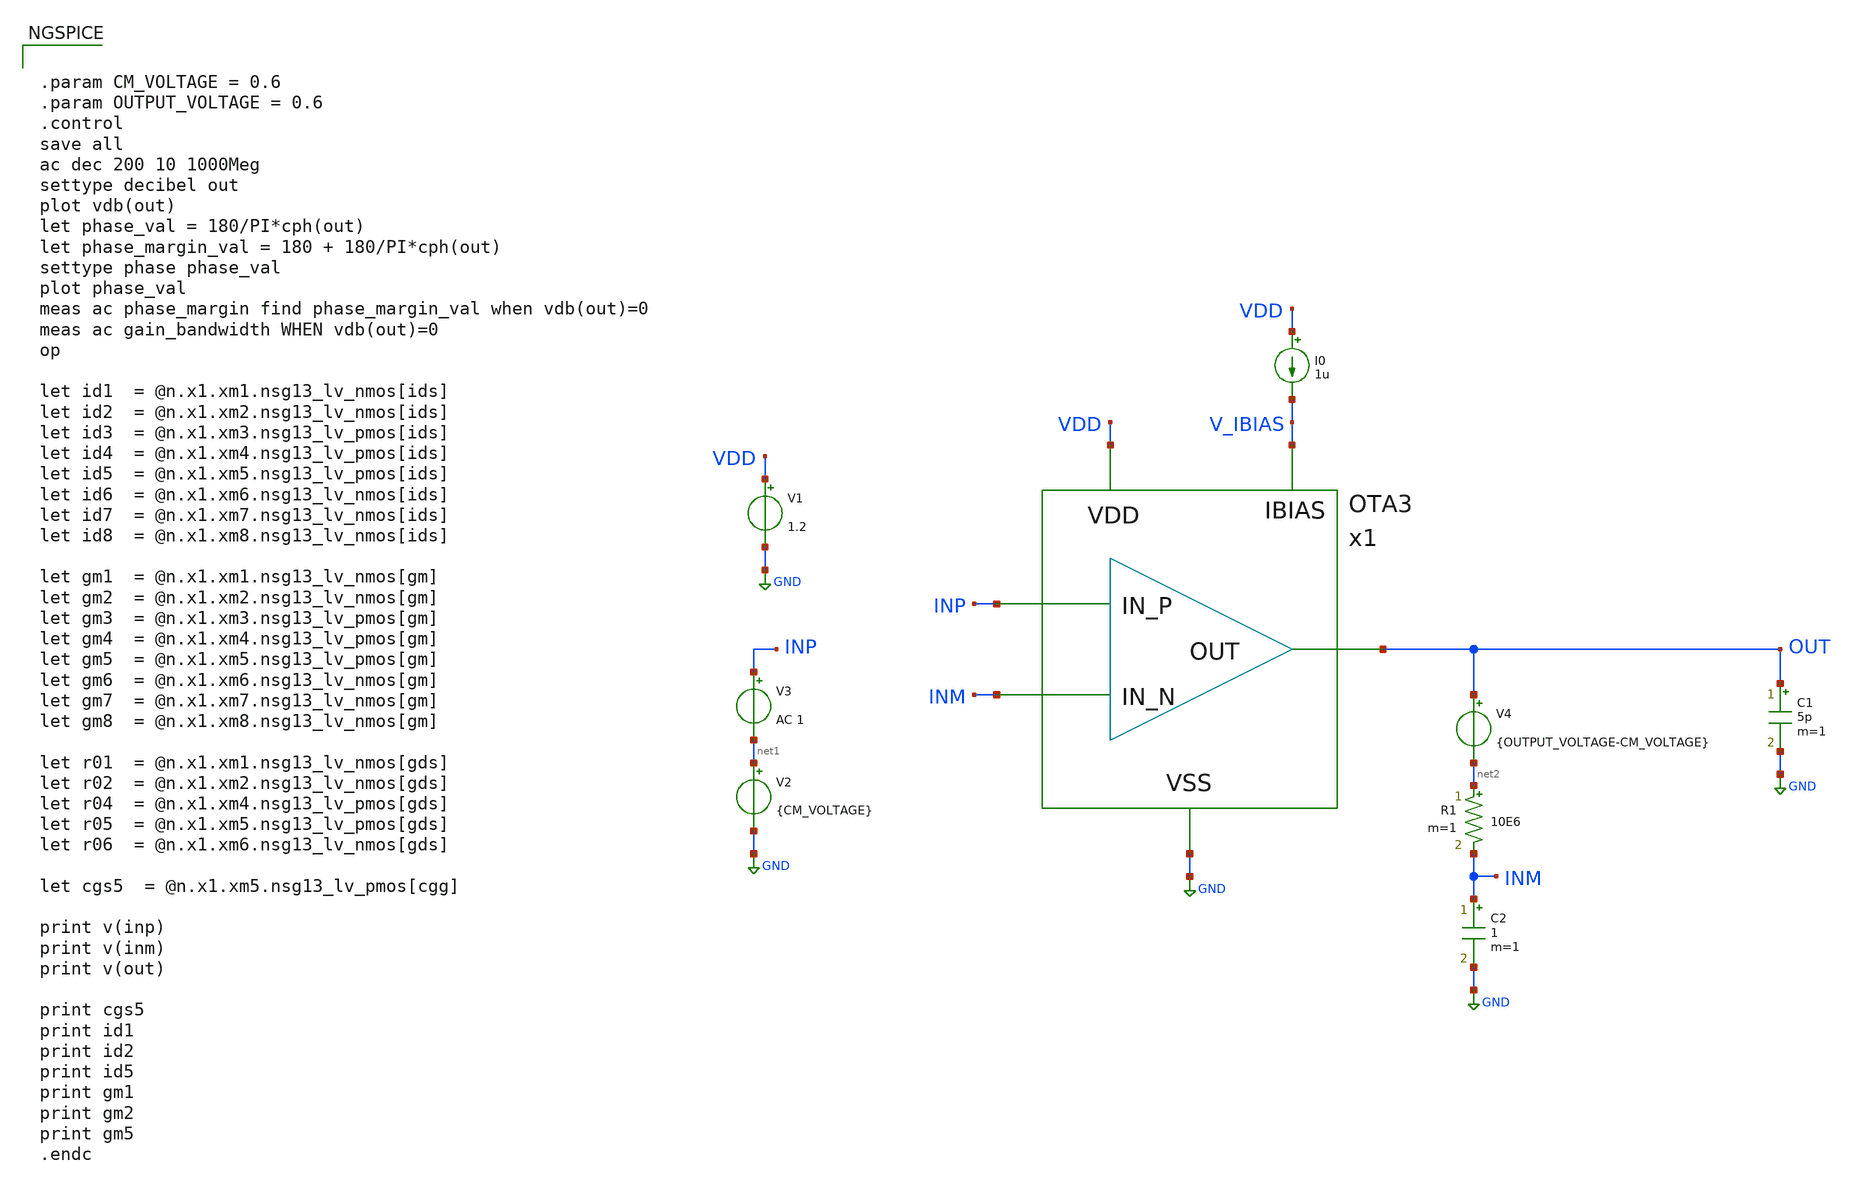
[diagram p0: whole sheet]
** sch_path: xschem/Tareas/Tarea_2/tb_OTA_lvt.sch
**.subckt tb_OTA_lvt
V1 VDD GND 1.2
I0 VDD V_IBIAS 1u
V2 net1 GND {CM_VOLTAGE}
V3 INP net1 AC 1
C1 OUT GND 5p m=1
R1 net2 INM 10E6 m=1
V4 OUT net2 {OUTPUT_VOLTAGE-CM_VOLTAGE}
C2 INM GND 1 m=1
x1 INP INM OUT VDD GND V_IBIAS OTA3
**** begin user architecture code


.param CM_VOLTAGE = 0.6
.param OUTPUT_VOLTAGE = 0.6
.control
save all
ac dec 200 10 1000Meg
settype decibel out
plot vdb(out)
let phase_val = 180/PI*cph(out)
let phase_margin_val = 180 + 180/PI*cph(out)
settype phase phase_val
plot phase_val
meas ac phase_margin find phase_margin_val when vdb(out)=0
meas ac gain_bandwidth WHEN vdb(out)=0
op

let id1  = @n.x1.xm1.nsg13_lv_nmos[ids]
let id2  = @n.x1.xm2.nsg13_lv_nmos[ids]
let id3  = @n.x1.xm3.nsg13_lv_pmos[ids]
let id4  = @n.x1.xm4.nsg13_lv_pmos[ids]
let id5  = @n.x1.xm5.nsg13_lv_pmos[ids]
let id6  = @n.x1.xm6.nsg13_lv_nmos[ids]
let id7  = @n.x1.xm7.nsg13_lv_nmos[ids]
let id8  = @n.x1.xm8.nsg13_lv_nmos[ids]

let gm1  = @n.x1.xm1.nsg13_lv_nmos[gm]
let gm2  = @n.x1.xm2.nsg13_lv_nmos[gm]
let gm3  = @n.x1.xm3.nsg13_lv_pmos[gm]
let gm4  = @n.x1.xm4.nsg13_lv_pmos[gm]
let gm5  = @n.x1.xm5.nsg13_lv_pmos[gm]
let gm6  = @n.x1.xm6.nsg13_lv_nmos[gm]
let gm7  = @n.x1.xm7.nsg13_lv_nmos[gm]
let gm8  = @n.x1.xm8.nsg13_lv_nmos[gm]

let r01  = @n.x1.xm1.nsg13_lv_nmos[gds]
let r02  = @n.x1.xm2.nsg13_lv_nmos[gds]
let r04  = @n.x1.xm4.nsg13_lv_pmos[gds]
let r05  = @n.x1.xm5.nsg13_lv_pmos[gds]
let r06  = @n.x1.xm6.nsg13_lv_nmos[gds]

let cgs5  = @n.x1.xm5.nsg13_lv_pmos[cgg]

print v(inp)
print v(inm)
print v(out)

print cgs5
print id1
print id2
print id5
print gm1
print gm2
print gm5
.endc




.lib cornerMOShv.lib mos_tt
.lib cornerMOSlv.lib mos_tt
*.lib cornerMOShv.lib mos_ff
*.lib cornerMOSlv.lib mos_ff
*.lib cornerMOShv.lib mos_ss
*.lib cornerMOSlv.lib mos_ss
*.lib cornerMOShv.lib mos_sf
*.lib cornerMOSlv.lib mos_sf
*.lib cornerMOShv.lib mos_fs
*.lib cornerMOSlv.lib mos_fs

.include /opt/pdks/ihp-sg13g2/libs.ref/sg13g2_stdcell/spice/sg13g2_stdcell.spice
.lib $::SG13G2_MODELS/cornerRES.lib res_typ
.lib $::SG13G2_MODELS/cornerCAP.lib cap_typ
*.lib $::SG13G2_MODELS/diodes.lib

**** end user architecture code
**.ends

* expanding   symbol:  OTA3.sym # of pins=6
** sym_path: xschem/Tareas/Tarea_2/OTA3.sym
** sch_path: xschem/Tareas/Tarea_2/OTA3.sch
.subckt OTA3 IN_P IN_N OUT VDD VSS ibias
*.ipin IN_N
*.ipin IN_P
*.opin OUT
*.ipin VDD
*.ipin VSS
*.ipin ibias
C2 OUT Vo1_p 1p m=1
XM8 ibias ibias VSS VSS sg13_lv_nmos w=1u l=0.5u ng=1 m=1 mm_ok=1
XM7 Vsrc ibias VSS VSS sg13_lv_nmos w=1.5u l=0.5u ng=1 m=1 mm_ok=1
XM6 OUT ibias VSS VSS sg13_lv_nmos w=1u l=0.5u ng=1 m=5 mm_ok=1
XM1 Vo1_n IN_N Vsrc VSS sg13_lv_nmos w=1u l=0.5u ng=1 m=1 mm_ok=1
XM2 Vo1_p IN_P Vsrc VSS sg13_lv_nmos w=1u l=0.5u ng=1 m=1 mm_ok=1
XM3 Vo1_n Vo1_n VDD VDD sg13_lv_pmos w=1u l=0.8u ng=1 m=1 mm_ok=1
XM4 Vo1_p Vo1_n VDD VDD sg13_lv_pmos w=1u l=0.8u ng=1 m=1 mm_ok=1
XM5 OUT Vo1_p VDD VDD sg13_lv_pmos w=5u l=0.5u ng=1 m=5 mm_ok=1
.ends

.GLOBAL GND
.end
